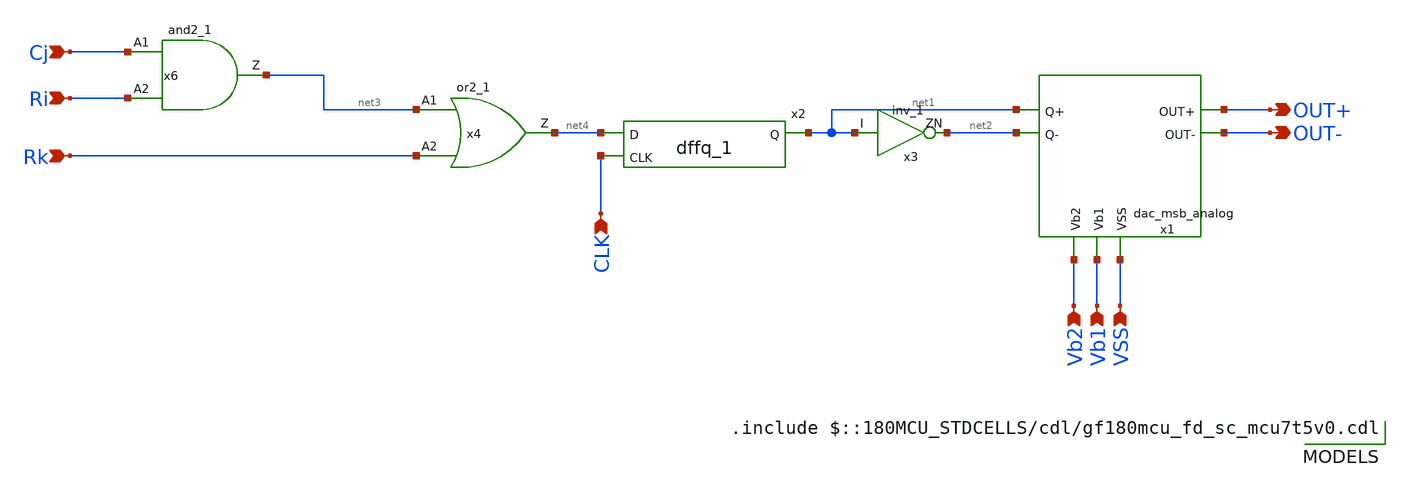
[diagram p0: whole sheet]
** sch_path: DAC/xschem/dac_msb_cell.sch
**.subckt dac_msb_cell Cj Rk Ri CLK Vb2 Vb1 VSS OUT+ OUT-
*.ipin Cj
*.ipin Rk
*.ipin Ri
*.ipin CLK
*.ipin Vb2
*.ipin Vb1
*.ipin VSS
*.opin OUT+
*.opin OUT-
x2 net4 CLK net1 DVDD DVDD DVSS DVSS gf180mcu_fd_sc_mcu7t5v0__dffq_1
x3 net1 net2 DVDD DVDD DVSS DVSS gf180mcu_fd_sc_mcu7t5v0__inv_1
x6 Cj Ri net3 DVDD DVDD DVSS DVSS gf180mcu_fd_sc_mcu7t5v0__and2_1
x4 net3 Rk net4 DVDD DVDD DVSS DVSS gf180mcu_fd_sc_mcu7t5v0__or2_1
x1 OUT+ OUT- net2 net1 Vb2 Vb1 VSS dac_msb_analog
**** begin user architecture code

.include $::180MCU_STDCELLS/cdl/gf180mcu_fd_sc_mcu7t5v0.cdl

**** end user architecture code
**.ends

* expanding   symbol:  dac_msb_analog.sym # of pins=7
** sym_path: DAC/xschem/dac_msb_analog.sym
** sch_path: DAC/xschem/dac_msb_analog.sch
.subckt dac_msb_analog OUT+ OUT- Q- Q+ Vb2 Vb1 VSS
*.ipin Q-
*.ipin Q+
*.ipin Vb1
*.ipin Vb2
*.opin OUT+
*.opin OUT-
*.ipin VSS
XM26 net1 Vb2 net2 VSS nfet_03v3 L=0.5u W=32u nf=16 ad='int((nf+1)/2) * W/nf * 0.18u' as='int((nf+2)/2) * W/nf * 0.18u'
+ pd='2*int((nf+1)/2) * (W/nf + 0.18u)' ps='2*int((nf+2)/2) * (W/nf + 0.18u)' nrd='0.18u / W' nrs='0.18u / W'
+ sa=0 sb=0 sd=0 m=1
XM27 net2 Vb1 VSS VSS nfet_03v3 L=0.5u W=32u nf=16 ad='int((nf+1)/2) * W/nf * 0.18u' as='int((nf+2)/2) * W/nf * 0.18u'
+ pd='2*int((nf+1)/2) * (W/nf + 0.18u)' ps='2*int((nf+2)/2) * (W/nf + 0.18u)' nrd='0.18u / W' nrs='0.18u / W'
+ sa=0 sb=0 sd=0 m=1
XM30 OUT+ Q+ net1 VSS nfet_03v3 L=0.5u W=16u nf=8 ad='int((nf+1)/2) * W/nf * 0.18u' as='int((nf+2)/2) * W/nf * 0.18u'
+ pd='2*int((nf+1)/2) * (W/nf + 0.18u)' ps='2*int((nf+2)/2) * (W/nf + 0.18u)' nrd='0.18u / W' nrs='0.18u / W'
+ sa=0 sb=0 sd=0 m=1
XM31 OUT- Q- net1 VSS nfet_03v3 L=0.5u W=16u nf=8 ad='int((nf+1)/2) * W/nf * 0.18u' as='int((nf+2)/2) * W/nf * 0.18u'
+ pd='2*int((nf+1)/2) * (W/nf + 0.18u)' ps='2*int((nf+2)/2) * (W/nf + 0.18u)' nrd='0.18u / W' nrs='0.18u / W'
+ sa=0 sb=0 sd=0 m=1
.ends

.end
